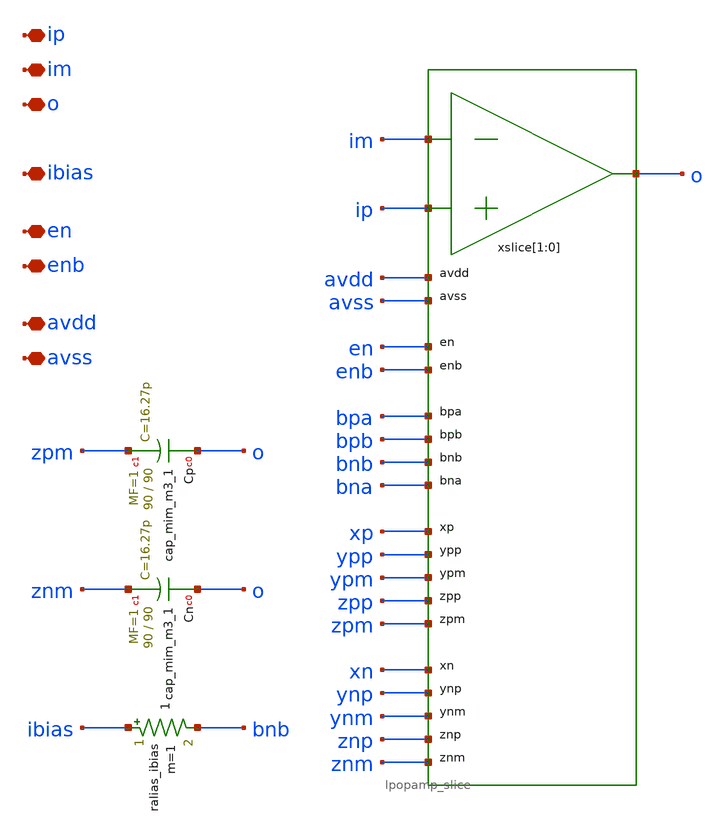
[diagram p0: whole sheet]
** sch_path: xschem/lpopamp.sch
**.subckt lpopamp avdd avss ip im o ibias en enb
*.iopin avdd
*.iopin avss
*.iopin ip
*.iopin im
*.iopin o
*.iopin ibias
*.iopin en
*.iopin enb
xslice[1] im ip o avdd avss en enb bpa bpb bnb bna xp ypp ypm zpp zpm xn ynp ynm znp znm
+ lpopamp_slice
xslice[0] im ip o avdd avss en enb bpa bpb bnb bna xp ypp ypm zpp zpm xn ynp ynm znp znm
+ lpopamp_slice
ralias_ibias ibias bnb 1 m=1
XCp o zpm sky130_fd_pr__cap_mim_m3_1 W=90 L=90 MF=1 m=1
XCn o znm sky130_fd_pr__cap_mim_m3_1 W=90 L=90 MF=1 m=1
**.ends
.end
